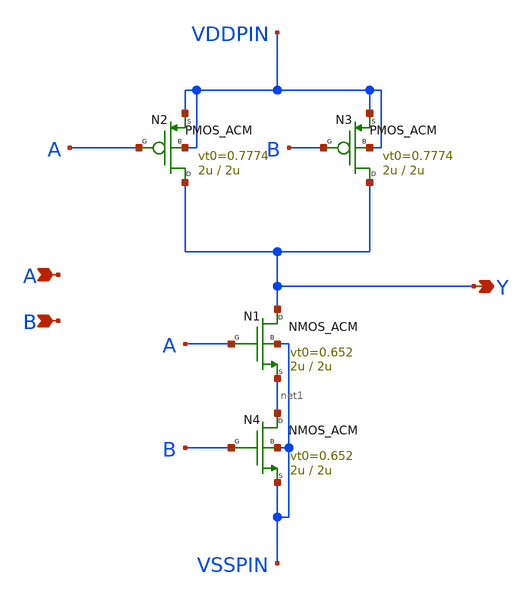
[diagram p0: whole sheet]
** sch_path: legacy/Examples/GF180MCU/xschem/symbol/nand2_acm.sch
**.subckt nand2_acm A Y B
*.ipin A
*.opin Y
*.ipin B
N1 Y A net1 VSSPIN NMOS_ACM w=2u l=2u n=1.38 is=67.3n vt0=0.652 sigma=20m zeta=5m
N2 Y A VDDPIN VDDPIN PMOS_ACM w=2u l=2u n=1.438 is=17.94n vt0=0.7774 sigma=20m zeta=5m
N3 Y B VDDPIN VDDPIN PMOS_ACM w=2u l=2u n=1.438 is=17.94n vt0=0.7774 sigma=20m zeta=5m
N4 net1 B VSSPIN VSSPIN NMOS_ACM w=2u l=2u n=1.38 is=67.3n vt0=0.652 sigma=20m zeta=5m
**.ends
.end
